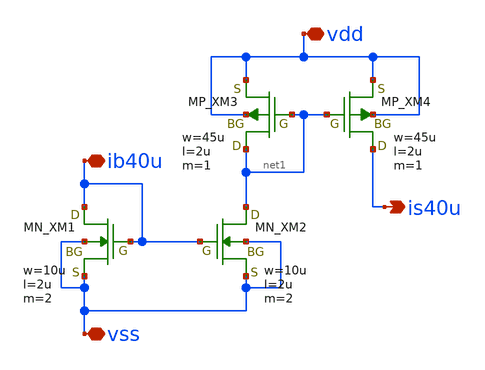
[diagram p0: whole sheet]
** sch_path: member_project/JJY_Receiver/Masahiro/jjy_recv/bias_for_mix_amp/bias40u.sch
**.subckt bias40u vss ib40u vdd is40u
*.iopin vss
*.iopin ib40u
*.iopin vdd
*.opin is40u
XXM1 ib40u ib40u vss vss NMOS w=10u l=2u nrd=0 nrs=0 m=2
XXM2 net1 ib40u vss vss NMOS w=10u l=2u nrd=0 nrs=0 m=2
XXM3 net1 net1 vdd vdd PMOS w=45u l=2u nrd=0 nrs=0 m=1
XXM4 is40u net1 vdd vdd PMOS w=45u l=2u nrd=0 nrs=0 m=1
**.ends
.end
